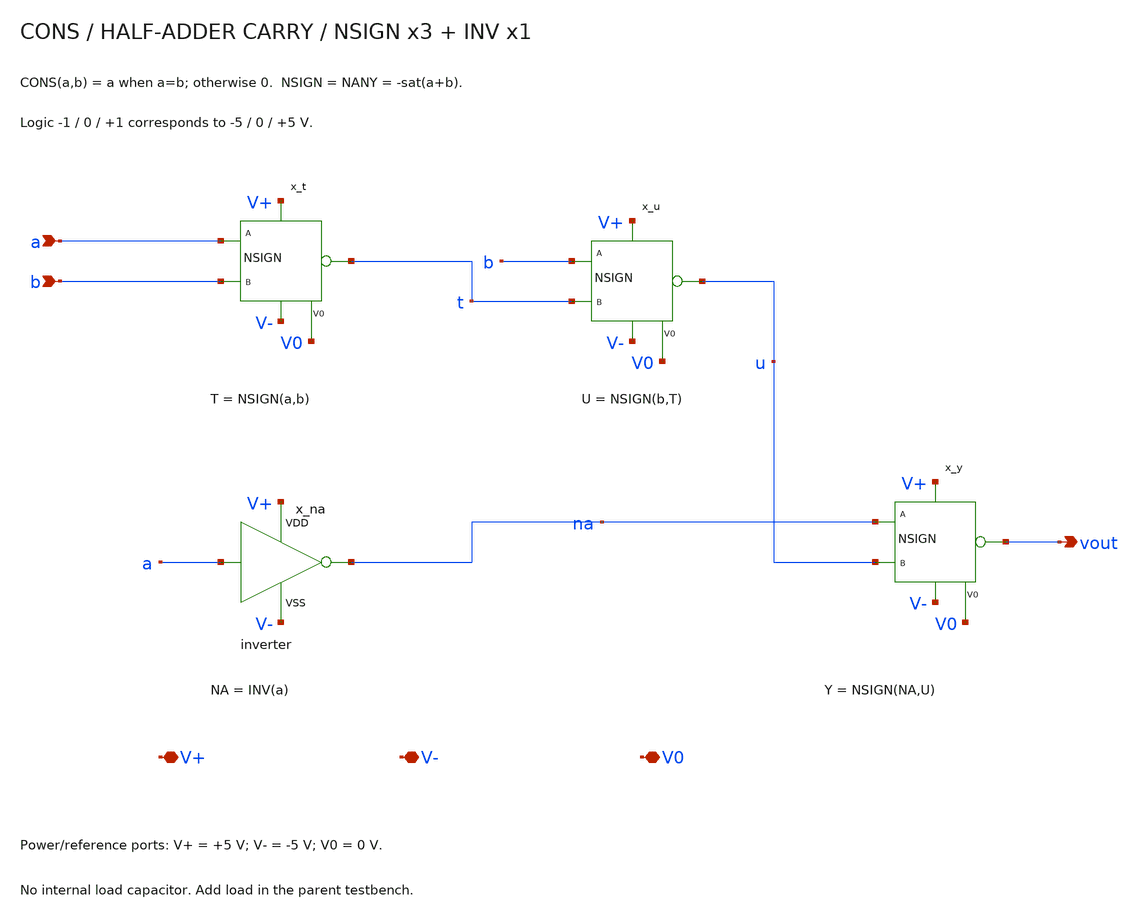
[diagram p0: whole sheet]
** sch_path: member_project/balanced-ternary-logic/PenguinEino/cons.sch
**.subckt cons a b vout V+ V- V0
*.ipin a
*.ipin b
*.opin vout
*.iopin V+
*.iopin V-
*.iopin V0
x_t a b t V+ V- V0 nsign
x_u b t u V+ V- V0 nsign
x_na a na V+ V- inverter
x_y na u vout V+ V- V0 nsign
**.ends

* expanding   symbol:  /home/ishi-kai/balanced-ternary-logic/nsign.sym # of pins=6
** sym_path: member_project/balanced-ternary-logic/PenguinEino/nsign.sym
** sch_path: member_project/balanced-ternary-logic/PenguinEino/nsign.sch
.subckt nsign a b vout V+ V- V0
*.iopin V+
*.ipin a
*.ipin b
*.opin vout
*.iopin V-
*.iopin V0
XXM3 net2 b net1 V+ PMOS w=34u l=1u nrd=0 nrs=0 m=1
XR2 net2 vout V+ F_RR w=2.8e-06 l=16e-06 R=1 tc1=0 tc2=0 m=1
XR1 vout net3 V+ F_RR w=2.8e-06 l=16e-06 R=1 tc1=0 tc2=0 m=1
XXM2 net3 a net4 V- NMOS w=11u l=1u nrd=0 nrs=0 m=1
XXM1 net4 b V- V- NMOS w=11u l=1u nrd=0 nrs=0 m=1
XXM5 net1 a V+ V+ PMOS w=34u l=1u nrd=0 nrs=0 m=1
XXM6 net5 a vout V+ PMOS w=14u l=1u nrd=0 nrs=0 m=1
XXM7 net5 b V0 V- NMOS w=8u l=1u nrd=0 nrs=0 m=1
XXM8 net6 b vout V+ PMOS w=14u l=1u nrd=0 nrs=0 m=1
XXM9 net6 a V0 V- NMOS w=8u l=1u nrd=0 nrs=0 m=1
.ends


* expanding   symbol:  /home/ishi-kai/balanced-ternary-logic/inverter.sym # of pins=4
** sym_path: member_project/balanced-ternary-logic/PenguinEino/inverter.sym
** sch_path: member_project/balanced-ternary-logic/PenguinEino/inverter.sch
.subckt inverter vin vout VDD VSS
*.iopin VDD
*.ipin vin
*.opin vout
*.iopin VSS
XXM1 net1 vin VDD VDD PMOS w=13.5u l=1u nrd=0 nrs=0 m=1
XR1 net1 vout VDD F_RR w=2.8e-06 l=30e-06 R=1 tc1=0 tc2=0 m=1
XR2 vout net2 VDD F_RR w=2.8e-06 l=30e-06 R=1 tc1=0 tc2=0 m=1
XXM2 net2 vin VSS VSS NMOS w=5u l=1u nrd=0 nrs=0 m=1
.ends

.end
